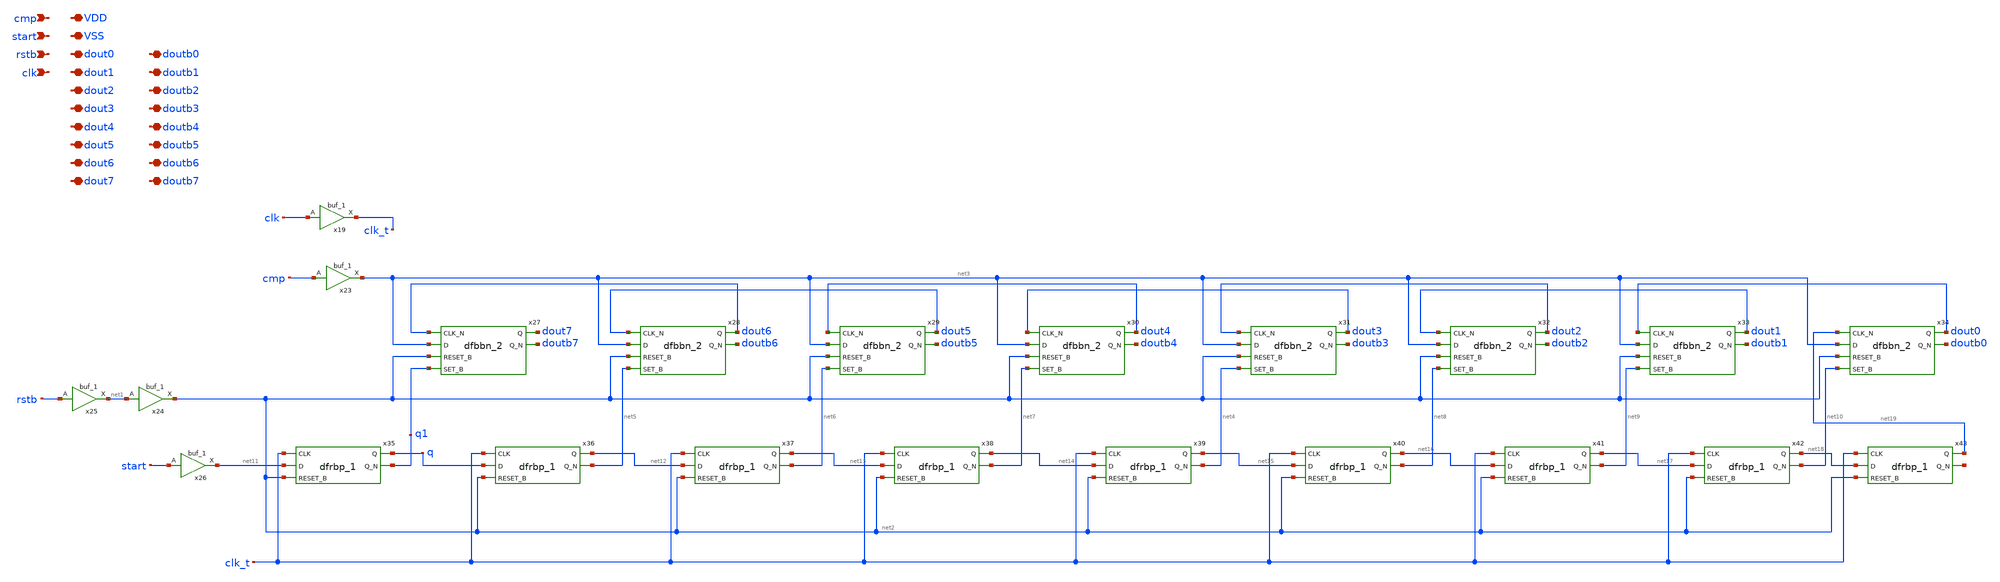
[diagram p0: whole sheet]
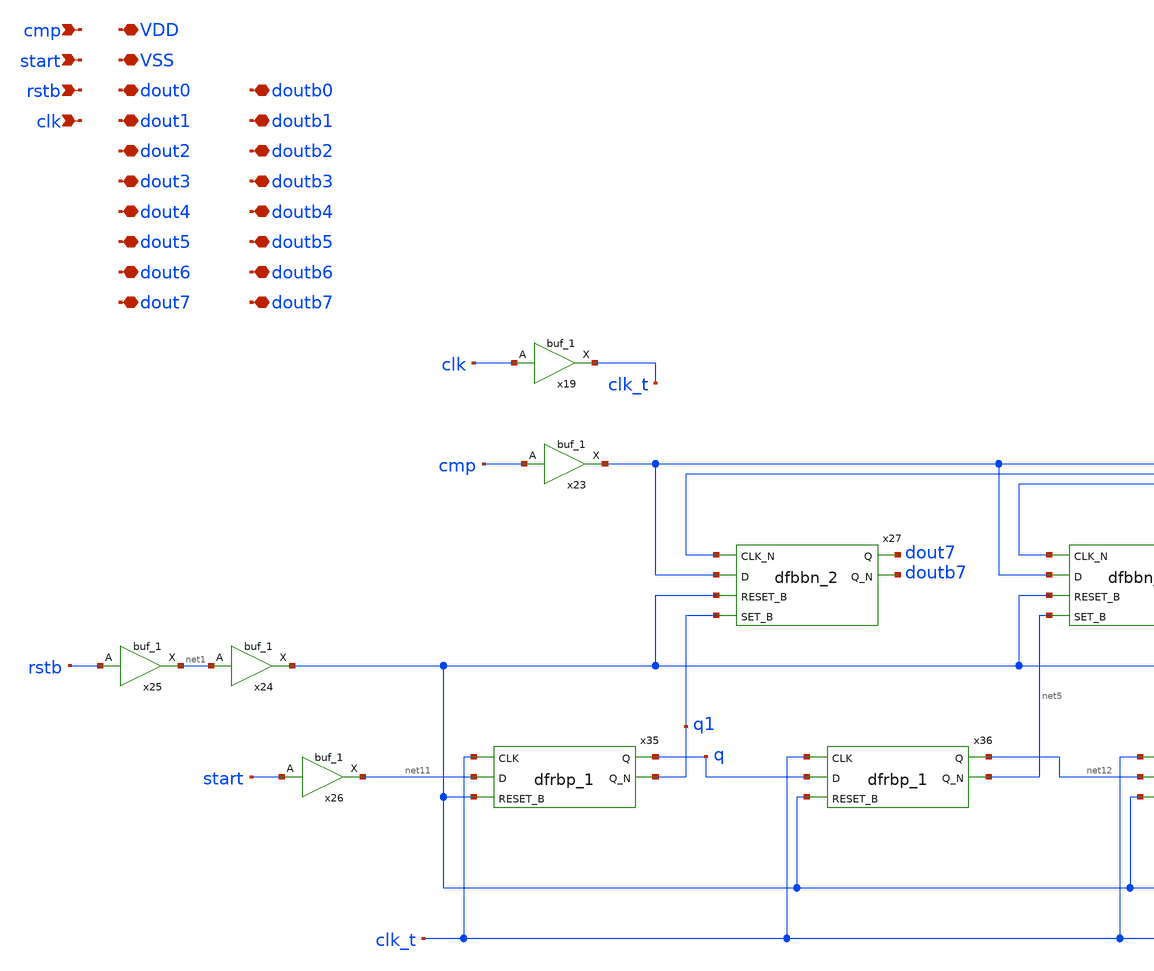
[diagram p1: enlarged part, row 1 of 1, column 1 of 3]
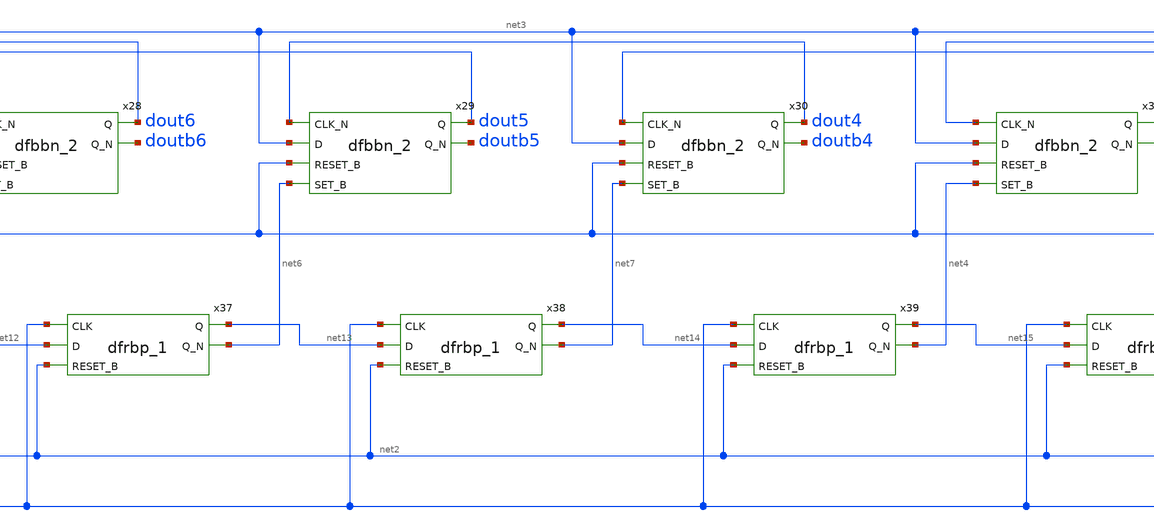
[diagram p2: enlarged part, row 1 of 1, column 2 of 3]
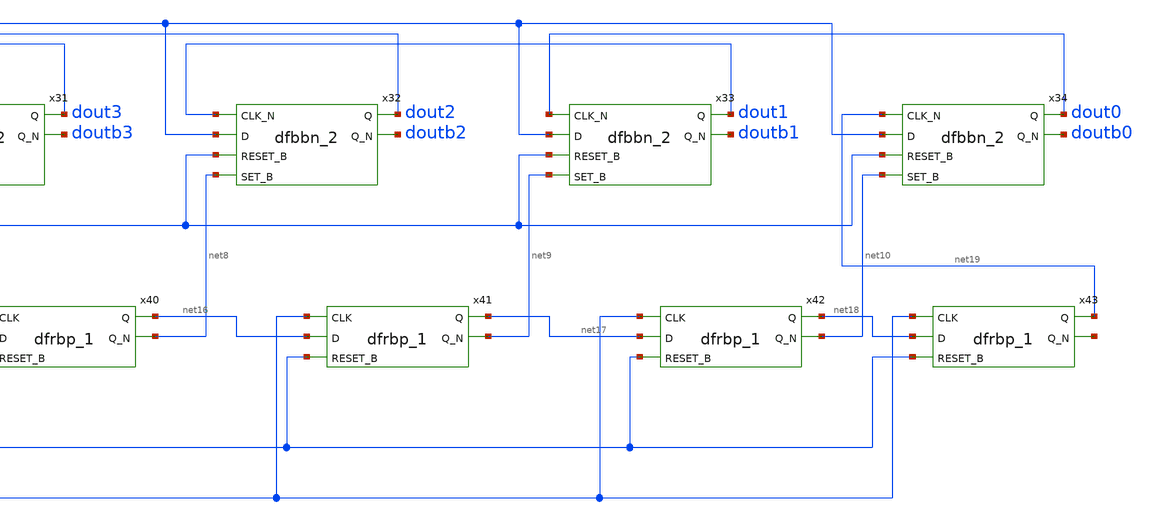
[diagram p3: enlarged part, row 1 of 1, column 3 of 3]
** sch_path: 8bitADC_SARLOGIC_pinout.sch
**.subckt 8bitADC_SARLOGIC_pinout cmp start rstb clk dout0 doutb0 VSS VDD dout1 dout2 dout3 dout4
*+ dout5 dout6 dout7 doutb1 doutb2 doutb3 doutb4 doutb5 doutb6 doutb7
*.ipin cmp
*.ipin start
*.ipin rstb
*.ipin clk
*.iopin dout0
*.iopin doutb0
*.iopin VSS
*.iopin VDD
*.iopin dout1
*.iopin dout2
*.iopin dout3
*.iopin dout4
*.iopin dout5
*.iopin dout6
*.iopin dout7
*.iopin doutb1
*.iopin doutb2
*.iopin doutb3
*.iopin doutb4
*.iopin doutb5
*.iopin doutb6
*.iopin doutb7
x19 clk VSS VNB VPB VDD clk_t sky130_fd_sc_hd__buf_1
x23 cmp VSS VNB VPB VDD net3 sky130_fd_sc_hd__buf_1
x24 net1 VSS VNB VPB VDD net2 sky130_fd_sc_hd__buf_1
x25 rstb VSS VNB VPB VDD net1 sky130_fd_sc_hd__buf_1
x26 start VSS VNB VPB VDD net11 sky130_fd_sc_hd__buf_1
x27 dout6 net3 net2 q1 VSS VNB VPB VDD dout7 doutb7 sky130_fd_sc_hd__dfbbn_2
x28 dout5 net3 net2 net5 VSS VNB VPB VDD dout6 doutb6 sky130_fd_sc_hd__dfbbn_2
x29 dout4 net3 net2 net6 VSS VNB VPB VDD dout5 doutb5 sky130_fd_sc_hd__dfbbn_2
x30 dout3 net3 net2 net7 VSS VNB VPB VDD dout4 doutb4 sky130_fd_sc_hd__dfbbn_2
x31 dout2 net3 net2 net4 VSS VNB VPB VDD dout3 doutb3 sky130_fd_sc_hd__dfbbn_2
x32 dout1 net3 net2 net8 VSS VNB VPB VDD dout2 doutb2 sky130_fd_sc_hd__dfbbn_2
x33 dout0 net3 net2 net9 VSS VNB VPB VDD dout1 doutb1 sky130_fd_sc_hd__dfbbn_2
x34 net19 net3 net2 net10 VSS VNB VPB VDD dout0 doutb0 sky130_fd_sc_hd__dfbbn_2
x35 clk_t net11 net2 VSS VNB VPB VDD q q1 sky130_fd_sc_hd__dfrbp_1
x36 clk_t q net2 VSS VNB VPB VDD net12 net5 sky130_fd_sc_hd__dfrbp_1
x37 clk_t net12 net2 VSS VNB VPB VDD net13 net6 sky130_fd_sc_hd__dfrbp_1
x38 clk_t net13 net2 VSS VNB VPB VDD net14 net7 sky130_fd_sc_hd__dfrbp_1
x39 clk_t net14 net2 VSS VNB VPB VDD net15 net4 sky130_fd_sc_hd__dfrbp_1
x40 clk_t net15 net2 VSS VNB VPB VDD net16 net8 sky130_fd_sc_hd__dfrbp_1
x41 clk_t net16 net2 VSS VNB VPB VDD net17 net9 sky130_fd_sc_hd__dfrbp_1
x42 clk_t net17 net2 VSS VNB VPB VDD net18 net10 sky130_fd_sc_hd__dfrbp_1
x43 clk_t net18 net2 VSS VNB VPB VDD net19 net20 sky130_fd_sc_hd__dfrbp_1
**.ends
.end
